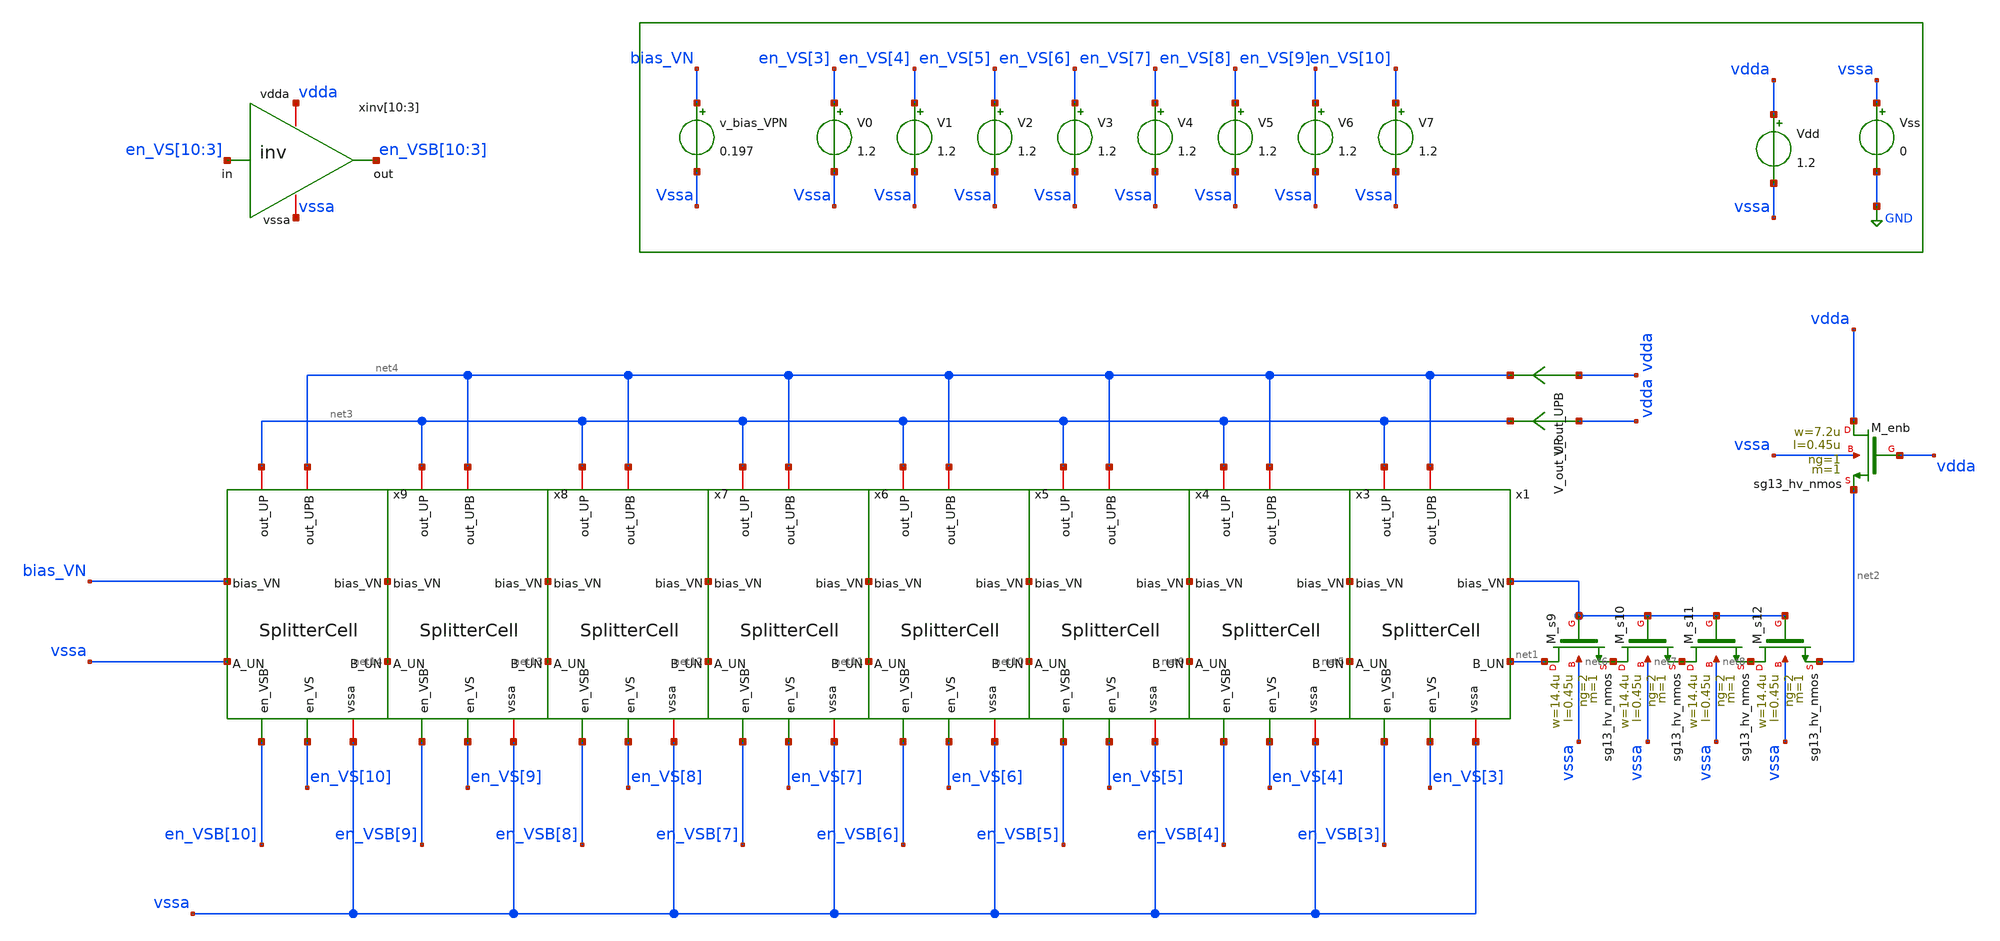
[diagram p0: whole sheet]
** sch_path: test_bench/CoreFineDAC_dc_tb.sch
**.subckt CoreFineDAC_dc_tb
x1 en_VS[3] net5 net1 en_VSB[3] bias_VN vssa net4 net3 SplitterCell
v_bias_VPN bias_VN Vssa 0.197
Vdd vdda vssa 1.2
V0 en_VS[3] Vssa 1.2
Vss vssa GND 0
XM_enb vdda vdda net2 vssa sg13_hv_nmos w=7.2u l=0.45u ng=1 m=1 mm_ok=1
XM_s9 net1 bias_VN net6 vssa sg13_hv_nmos w=14.4u l=0.45u ng=2 m=1 mm_ok=1
XM_s10 net6 bias_VN net7 vssa sg13_hv_nmos w=14.4u l=0.45u ng=2 m=1 mm_ok=1
XM_s11 net7 bias_VN net8 vssa sg13_hv_nmos w=14.4u l=0.45u ng=2 m=1 mm_ok=1
XM_s12 net8 bias_VN net2 vssa sg13_hv_nmos w=14.4u l=0.45u ng=2 m=1 mm_ok=1
xinv[10] vdda en_VSB[10] en_VS[10] vssa inv
xinv[9] vdda en_VSB[9] en_VS[9] vssa inv
xinv[8] vdda en_VSB[8] en_VS[8] vssa inv
xinv[7] vdda en_VSB[7] en_VS[7] vssa inv
xinv[6] vdda en_VSB[6] en_VS[6] vssa inv
xinv[5] vdda en_VSB[5] en_VS[5] vssa inv
xinv[4] vdda en_VSB[4] en_VS[4] vssa inv
xinv[3] vdda en_VSB[3] en_VS[3] vssa inv
V_out_UPB vdda net4 0
.save i(v_out_upb)
V_out_UP vdda net3 0
.save i(v_out_up)
x3 en_VS[4] net9 net5 en_VSB[4] bias_VN vssa net4 net3 SplitterCell
x4 en_VS[5] net10 net9 en_VSB[5] bias_VN vssa net4 net3 SplitterCell
x5 en_VS[6] net11 net10 en_VSB[6] bias_VN vssa net4 net3 SplitterCell
x6 en_VS[7] net12 net11 en_VSB[7] bias_VN vssa net4 net3 SplitterCell
x7 en_VS[8] net13 net12 en_VSB[8] bias_VN vssa net4 net3 SplitterCell
x8 en_VS[9] net14 net13 en_VSB[9] bias_VN vssa net4 net3 SplitterCell
x9 en_VS[10] vssa net14 en_VSB[10] bias_VN vssa net4 net3 SplitterCell
V1 en_VS[4] Vssa 1.2
V2 en_VS[5] Vssa 1.2
V3 en_VS[6] Vssa 1.2
V4 en_VS[7] Vssa 1.2
V5 en_VS[8] Vssa 1.2
V6 en_VS[9] Vssa 1.2
V7 en_VS[10] Vssa 1.2
**** begin user architecture code

.lib cornerMOShv.lib mos_tt



.param temp=27

.options abstol=1e-16
.options gmin=1e-16
.control

let digitalCommand = vector(256)
let out_UP   = vector(256)

let code = 0

while code < 256

    * Set the 8 bits
    alter V0 = 1.2*(code % 2)
    alter V1 = 1.2*(floor(code/2) % 2)
    alter V2 = 1.2*(floor(code/4) % 2)
    alter V3 = 1.2*(floor(code/8) % 2)
    alter V4 = 1.2*(floor(code/16) % 2)
    alter V5 = 1.2*(floor(code/32) % 2)
    alter V6 = 1.2*(floor(code/64) % 2)
    alter V7 = 1.2*(floor(code/128) % 2)

    op

    let digitalCommand[code] = code
    let out_UP[code]   = 0
    let out_UP[code]   = I(V_out_UP)
    let code = code + 1
end

    setplot const
    settype current out_UP
    setscale digitalCommand
    plot out_UP
    write SpllitterFull_10p_dc_tb.raw out_UP

.endc


**** end user architecture code
**.ends
.GLOBAL GND
.end
